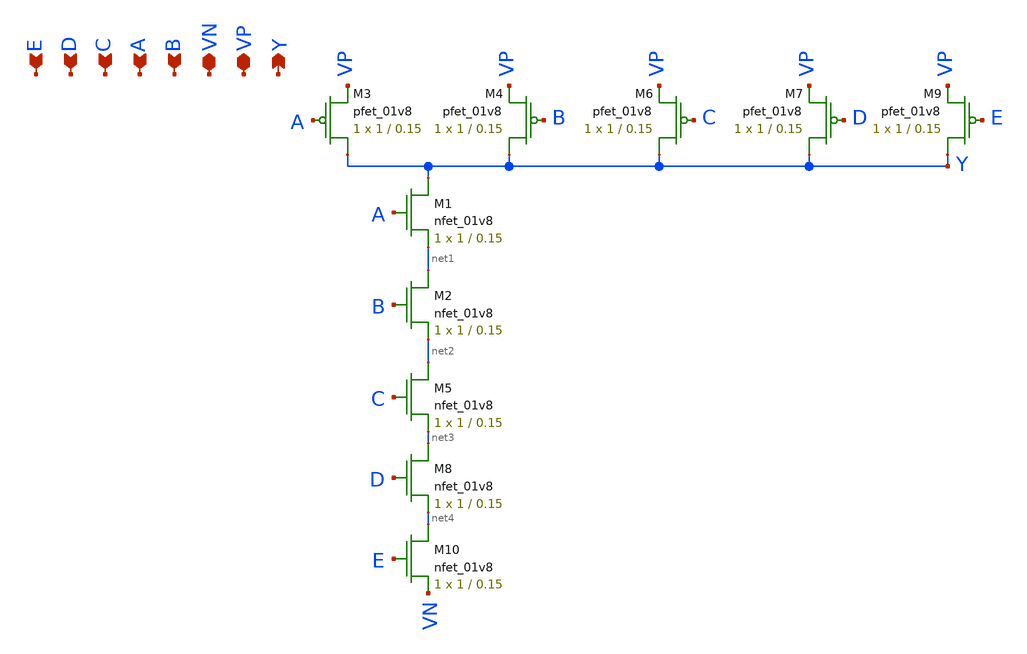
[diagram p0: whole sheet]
** sch_path: xschem/logic_gates/nand5.sch
**.subckt nand5 VP VN A B Y C D E
*.iopin VP
*.iopin VN
*.ipin A
*.ipin B
*.opin Y
*.ipin C
*.ipin D
*.ipin E
XM1 Y A net1 GND sky130_fd_pr__nfet_01v8 L=0.15 W=1 nf=1 ad='int((nf+1)/2) * W/nf * 0.29' as='int((nf+2)/2) * W/nf * 0.29'
+ pd='2*int((nf+1)/2) * (W/nf + 0.29)' ps='2*int((nf+2)/2) * (W/nf + 0.29)' nrd='0.29 / W' nrs='0.29 / W'
+ sa=0 sb=0 sd=0 mult=1 m=1
XM2 net1 B net2 GND sky130_fd_pr__nfet_01v8 L=0.15 W=1 nf=1 ad='int((nf+1)/2) * W/nf * 0.29' as='int((nf+2)/2) * W/nf * 0.29'
+ pd='2*int((nf+1)/2) * (W/nf + 0.29)' ps='2*int((nf+2)/2) * (W/nf + 0.29)' nrd='0.29 / W' nrs='0.29 / W'
+ sa=0 sb=0 sd=0 mult=1 m=1
XM3 Y A VP VDD sky130_fd_pr__pfet_01v8 L=0.15 W=1 nf=1 ad='int((nf+1)/2) * W/nf * 0.29' as='int((nf+2)/2) * W/nf * 0.29'
+ pd='2*int((nf+1)/2) * (W/nf + 0.29)' ps='2*int((nf+2)/2) * (W/nf + 0.29)' nrd='0.29 / W' nrs='0.29 / W'
+ sa=0 sb=0 sd=0 mult=1 m=1
XM4 Y B VP VDD sky130_fd_pr__pfet_01v8 L=0.15 W=1 nf=1 ad='int((nf+1)/2) * W/nf * 0.29' as='int((nf+2)/2) * W/nf * 0.29'
+ pd='2*int((nf+1)/2) * (W/nf + 0.29)' ps='2*int((nf+2)/2) * (W/nf + 0.29)' nrd='0.29 / W' nrs='0.29 / W'
+ sa=0 sb=0 sd=0 mult=1 m=1
XM5 net2 C net3 GND sky130_fd_pr__nfet_01v8 L=0.15 W=1 nf=1 ad='int((nf+1)/2) * W/nf * 0.29' as='int((nf+2)/2) * W/nf * 0.29'
+ pd='2*int((nf+1)/2) * (W/nf + 0.29)' ps='2*int((nf+2)/2) * (W/nf + 0.29)' nrd='0.29 / W' nrs='0.29 / W'
+ sa=0 sb=0 sd=0 mult=1 m=1
XM6 Y C VP VDD sky130_fd_pr__pfet_01v8 L=0.15 W=1 nf=1 ad='int((nf+1)/2) * W/nf * 0.29' as='int((nf+2)/2) * W/nf * 0.29'
+ pd='2*int((nf+1)/2) * (W/nf + 0.29)' ps='2*int((nf+2)/2) * (W/nf + 0.29)' nrd='0.29 / W' nrs='0.29 / W'
+ sa=0 sb=0 sd=0 mult=1 m=1
XM7 Y D VP VDD sky130_fd_pr__pfet_01v8 L=0.15 W=1 nf=1 ad='int((nf+1)/2) * W/nf * 0.29' as='int((nf+2)/2) * W/nf * 0.29'
+ pd='2*int((nf+1)/2) * (W/nf + 0.29)' ps='2*int((nf+2)/2) * (W/nf + 0.29)' nrd='0.29 / W' nrs='0.29 / W'
+ sa=0 sb=0 sd=0 mult=1 m=1
XM8 net3 D net4 GND sky130_fd_pr__nfet_01v8 L=0.15 W=1 nf=1 ad='int((nf+1)/2) * W/nf * 0.29' as='int((nf+2)/2) * W/nf * 0.29'
+ pd='2*int((nf+1)/2) * (W/nf + 0.29)' ps='2*int((nf+2)/2) * (W/nf + 0.29)' nrd='0.29 / W' nrs='0.29 / W'
+ sa=0 sb=0 sd=0 mult=1 m=1
XM9 Y E VP VDD sky130_fd_pr__pfet_01v8 L=0.15 W=1 nf=1 ad='int((nf+1)/2) * W/nf * 0.29' as='int((nf+2)/2) * W/nf * 0.29'
+ pd='2*int((nf+1)/2) * (W/nf + 0.29)' ps='2*int((nf+2)/2) * (W/nf + 0.29)' nrd='0.29 / W' nrs='0.29 / W'
+ sa=0 sb=0 sd=0 mult=1 m=1
XM10 net4 E VN GND sky130_fd_pr__nfet_01v8 L=0.15 W=1 nf=1 ad='int((nf+1)/2) * W/nf * 0.29' as='int((nf+2)/2) * W/nf * 0.29'
+ pd='2*int((nf+1)/2) * (W/nf + 0.29)' ps='2*int((nf+2)/2) * (W/nf + 0.29)' nrd='0.29 / W' nrs='0.29 / W'
+ sa=0 sb=0 sd=0 mult=1 m=1
**.ends
.end
